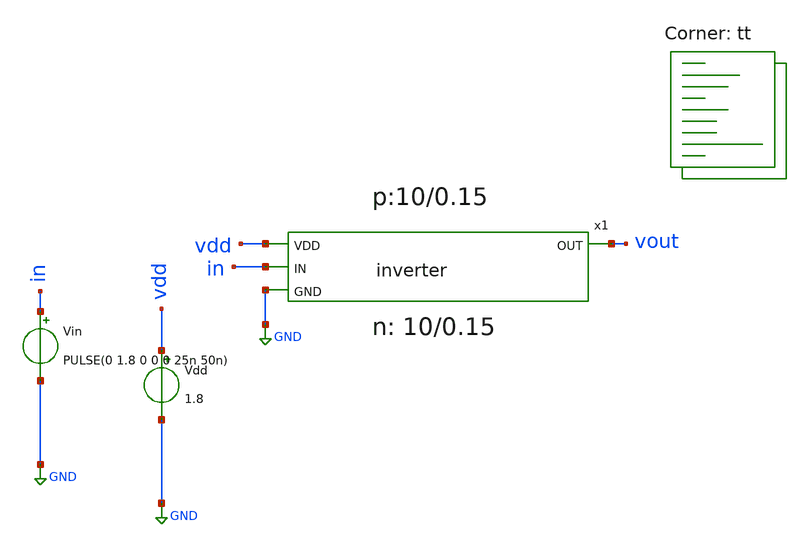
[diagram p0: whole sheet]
** sch_path: tb_inverter.sch
**.subckt tb_inverter
Vin in GND PULSE(0 1.8 0 0 0 25n 50n)
Vdd vdd GND 1.8
x1 vdd vout in GND inverter
**** begin user architecture code



.options savecurrents


.param pmos_width=10

.control
save all


let step=1
let max_w=80
let curr_w=40
let min_diff=100
let best_w=100



while curr_w < max_w


	alterparam pmos_width = curr_w
	reset
	tran 10p 50n


	meas tran rise_time TRIG v(vout) VAL=0.18 RISE=1 TARG v(vout) VAL=1.62 RISE=1
	meas tran fall_time TRIG v(vout) VAL=1.62 FALL=1 TARG v(vout) VAL=0.18 FALL=1


	let diff_rise_fall=abs(rise_time - fall_time)

	if diff_rise_fall < min_diff
		let best_w = curr_w
		let min_diff = diff_rise_fall
	end

	print diff_rise_fall

	let curr_w=curr_w + step


end

print min_diff
print best_w

.endc


.lib $::SKYWATER_MODELS/sky130.lib.spice tt
**** end user architecture code
**.ends

* expanding   symbol:  inverter.sym # of pins=4
** sym_path: inverter.sym
** sch_path: inverter.sch
.subckt inverter VDD OUT IN GND
*.ipin IN
*.ipin VDD
*.opin OUT
*.ipin GND
XM2 OUT IN GND GND sky130_fd_pr__nfet_01v8 L='ln' W='wn' nf=1 ad='int((nf+1)/2) * W/nf * 0.29' as='int((nf+2)/2) * W/nf * 0.29'
+ pd='2*int((nf+1)/2) * (W/nf + 0.29)' ps='2*int((nf+2)/2) * (W/nf + 0.29)' nrd='0.29 / W' nrs='0.29 / W'
+ sa=0 sb=0 sd=0 mult=1 m=1
XM1 OUT IN VDD VDD sky130_fd_pr__pfet_01v8 L='lp' W='wp' nf=1 ad='int((nf+1)/2) * W/nf * 0.29' as='int((nf+2)/2) * W/nf * 0.29'
+ pd='2*int((nf+1)/2) * (W/nf + 0.29)' ps='2*int((nf+2)/2) * (W/nf + 0.29)' nrd='0.29 / W' nrs='0.29 / W'
+ sa=0 sb=0 sd=0 mult=1 m=1
.ends

.GLOBAL GND
.end
